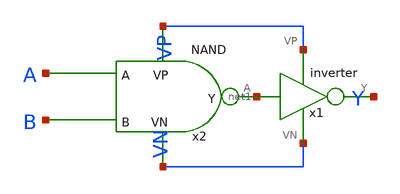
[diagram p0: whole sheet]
** sch_path: MADVLSI_MP1/AND_LVS.sch
**.subckt AND_LVS
x1 VP net1 Y VN inverter
x2 VP A B net1 VN NAND
**.ends

* expanding   symbol:  /home/allan/Documents/MADVLSI_MP1/inverter.sym # of pins=4
** sym_path: MADVLSI_MP1/inverter.sym
** sch_path: MADVLSI_MP1/inverter.sch
.subckt inverter VP A Y VN
*.ipin A
*.iopin VP
*.iopin VN
*.opin Y
XM1 Y A VN VN sky130_fd_pr__nfet_01v8 L=0.15 W=1 nf=1 ad='int((nf+1)/2) * W/nf * 0.29' as='int((nf+2)/2) * W/nf * 0.29'
+ pd='2*int((nf+1)/2) * (W/nf + 0.29)' ps='2*int((nf+2)/2) * (W/nf + 0.29)' nrd='0.29 / W' nrs='0.29 / W'
+ sa=0 sb=0 sd=0 mult=1 m=1
XM2 Y A VP VP sky130_fd_pr__pfet_01v8 L=0.15 W=1 nf=1 ad='int((nf+1)/2) * W/nf * 0.29' as='int((nf+2)/2) * W/nf * 0.29'
+ pd='2*int((nf+1)/2) * (W/nf + 0.29)' ps='2*int((nf+2)/2) * (W/nf + 0.29)' nrd='0.29 / W' nrs='0.29 / W'
+ sa=0 sb=0 sd=0 mult=1 m=1
.ends


* expanding   symbol:  /home/allan/Documents/MADVLSI_MP1/NAND.sym # of pins=5
** sym_path: MADVLSI_MP1/NAND.sym
** sch_path: MADVLSI_MP1/NAND.sch
.subckt NAND VP A B Y VN
*.ipin A
*.ipin B
*.iopin VP
*.iopin VN
*.opin Y
XM1 Y A VP VP sky130_fd_pr__pfet_01v8 L=0.15 W=1 nf=1 ad='int((nf+1)/2) * W/nf * 0.29' as='int((nf+2)/2) * W/nf * 0.29'
+ pd='2*int((nf+1)/2) * (W/nf + 0.29)' ps='2*int((nf+2)/2) * (W/nf + 0.29)' nrd='0.29 / W' nrs='0.29 / W'
+ sa=0 sb=0 sd=0 mult=1 m=1
XM2 VP B Y VP sky130_fd_pr__pfet_01v8 L=0.15 W=1 nf=1 ad='int((nf+1)/2) * W/nf * 0.29' as='int((nf+2)/2) * W/nf * 0.29'
+ pd='2*int((nf+1)/2) * (W/nf + 0.29)' ps='2*int((nf+2)/2) * (W/nf + 0.29)' nrd='0.29 / W' nrs='0.29 / W'
+ sa=0 sb=0 sd=0 mult=1 m=1
XM3 Y A net1 VN sky130_fd_pr__nfet_01v8 L=0.15 W=1 nf=1 ad='int((nf+1)/2) * W/nf * 0.29' as='int((nf+2)/2) * W/nf * 0.29'
+ pd='2*int((nf+1)/2) * (W/nf + 0.29)' ps='2*int((nf+2)/2) * (W/nf + 0.29)' nrd='0.29 / W' nrs='0.29 / W'
+ sa=0 sb=0 sd=0 mult=1 m=1
XM4 net1 B VN VN sky130_fd_pr__nfet_01v8 L=0.15 W=1 nf=1 ad='int((nf+1)/2) * W/nf * 0.29' as='int((nf+2)/2) * W/nf * 0.29'
+ pd='2*int((nf+1)/2) * (W/nf + 0.29)' ps='2*int((nf+2)/2) * (W/nf + 0.29)' nrd='0.29 / W' nrs='0.29 / W'
+ sa=0 sb=0 sd=0 mult=1 m=1
.ends

.end
